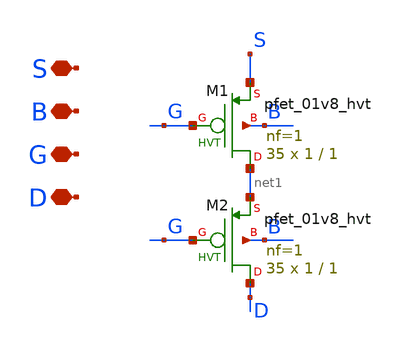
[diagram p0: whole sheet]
** sch_path: xschem/INA/Transistors/transistors_bias_network/pfet_m12_to_m14.sch
**.subckt pfet_m12_to_m14 S B G D
*.iopin S
*.iopin B
*.iopin G
*.iopin D
XM1 net1 G S B sky130_fd_pr__pfet_01v8_hvt L=1 W=1 nf=1 ad='int((nf+1)/2) * W/nf * 0.29' as='int((nf+2)/2) * W/nf * 0.29'
+ pd='2*int((nf+1)/2) * (W/nf + 0.29)' ps='2*int((nf+2)/2) * (W/nf + 0.29)' nrd='0.29 / W' nrs='0.29 / W'
+ sa=0 sb=0 sd=0 mult=35 m=35
XM2 D G net1 B sky130_fd_pr__pfet_01v8_hvt L=1 W=1 nf=1 ad='int((nf+1)/2) * W/nf * 0.29' as='int((nf+2)/2) * W/nf * 0.29'
+ pd='2*int((nf+1)/2) * (W/nf + 0.29)' ps='2*int((nf+2)/2) * (W/nf + 0.29)' nrd='0.29 / W' nrs='0.29 / W'
+ sa=0 sb=0 sd=0 mult=35 m=35
**.ends
.end
